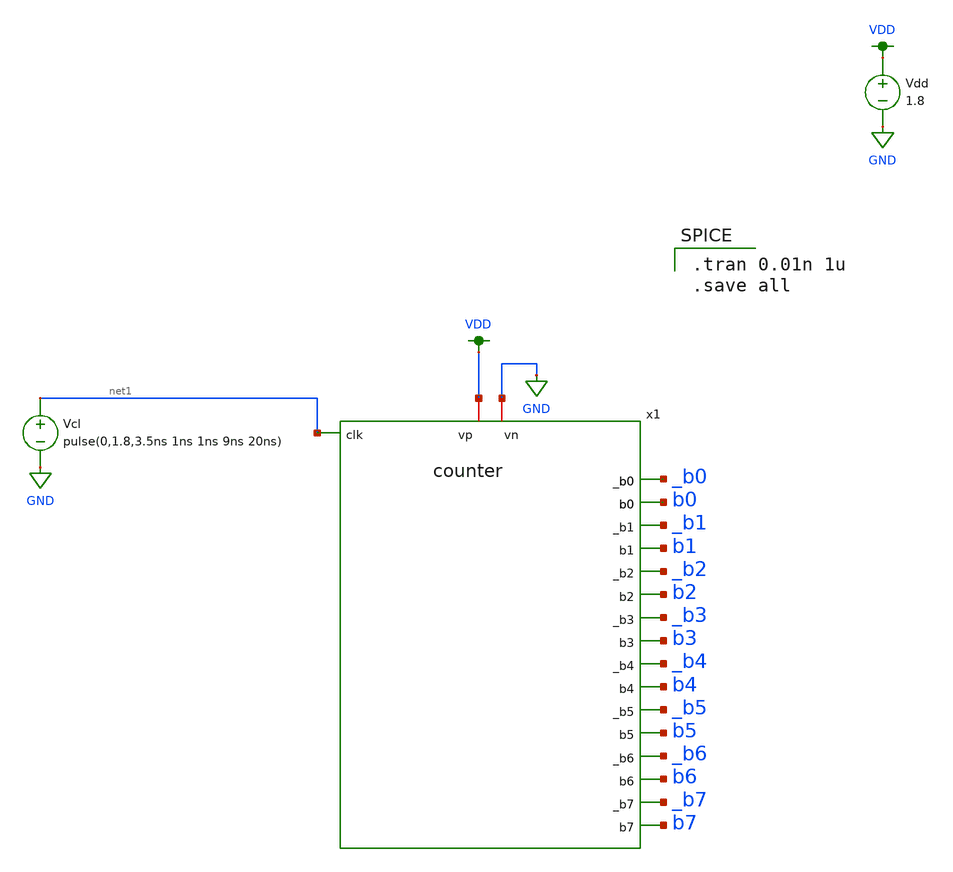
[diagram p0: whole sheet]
** sch_path: xschem/counter_testbench.sch
**.subckt counter_testbench
Vdd VDD GND 1.8
Vcl net1 GND pulse(0,1.8,3.5ns 1ns 1ns 9ns 20ns)
x1 VDD GND net1 _b1 b1 _b2 b2 _b3 b3 _b0 b0 _b5 b5 _b6 b6 _b7 b7 _b4 b4 counter
**** begin user architecture code

.option wnflag=1
.param MC_SWITCH=1.0
.lib ~/skywater/skywater-pdk/libraries/sky130_fd_pr_ngspice/latest/models/sky130.lib.spice tt


.tran 0.01n 1u
.save all

**** end user architecture code
**.ends

* expanding   symbol:  /home/madvlsi/dev/git/magic-dds/xschem/logic_gates/counter.sym # of pins=19
** sym_path: xschem/logic_gates/counter.sym
** sch_path: xschem/logic_gates/counter.sch
.subckt counter vp vn clk _b1 b1 _b2 b2 _b3 b3 _b0 b0 _b5 b5 _b6 b6 _b7 b7 _b4 b4
*.iopin vp
*.iopin vn
*.ipin clk
*.opin b0
*.opin _b0
*.opin b1
*.opin _b1
*.opin b2
*.opin _b2
*.opin b3
*.opin _b3
*.opin b4
*.opin _b4
*.opin b5
*.opin _b5
*.opin b6
*.opin _b6
*.opin b7
*.opin _b7
X2 _b1 b1 _b1 b1 _b0 vp vn dflipflop
X3 _b2 b2 _b2 b2 _b1 vp vn dflipflop
X4 _b3 b3 _b3 b3 _b2 vp vn dflipflop
X5 _b4 b4 _b4 b4 _b3 vp vn dflipflop
X6 _b5 b5 _b5 b5 _b4 vp vn dflipflop
X7 _b6 b6 _b6 b6 _b5 vp vn dflipflop
X8 _b7 b7 _b7 b7 _b6 vp vn dflipflop
x9 vp clk _b0 vn inverter
x10 vp _b0 b0 vn inverter
.ends


* expanding   symbol:  /home/madvlsi/dev/git/magic-dds/xschem/logic_gates/dflipflop.sym # of pins=7
** sym_path: xschem/logic_gates/dflipflop.sym
** sch_path: xschem/logic_gates/dflipflop.sch
.subckt dflipflop q_bar q d d_bar clk vp vn
*.opin q
*.opin q_bar
*.iopin vp
*.iopin vn
*.ipin d_bar
*.ipin d
*.ipin clk
XM8 vp net2 net3 vp sky130_fd_pr__pfet_01v8 L=0.15 W=1 nf=1 ad='int((nf+1)/2) * W/nf * 0.29' as='int((nf+2)/2) * W/nf * 0.29'
+ pd='2*int((nf+1)/2) * (W/nf + 0.29)' ps='2*int((nf+2)/2) * (W/nf + 0.29)' nrd='0.29 / W' nrs='0.29 / W'
+ sa=0 sb=0 sd=0 mult=1 m=1
XM9 vp net3 net2 vp sky130_fd_pr__pfet_01v8 L=0.15 W=1 nf=1 ad='int((nf+1)/2) * W/nf * 0.29' as='int((nf+2)/2) * W/nf * 0.29'
+ pd='2*int((nf+1)/2) * (W/nf + 0.29)' ps='2*int((nf+2)/2) * (W/nf + 0.29)' nrd='0.29 / W' nrs='0.29 / W'
+ sa=0 sb=0 sd=0 mult=1 m=1
XM5 net1 clk vn vn sky130_fd_pr__nfet_01v8 L=0.15 W=1 nf=1 ad='int((nf+1)/2) * W/nf * 0.29' as='int((nf+2)/2) * W/nf * 0.29'
+ pd='2*int((nf+1)/2) * (W/nf + 0.29)' ps='2*int((nf+2)/2) * (W/nf + 0.29)' nrd='0.29 / W' nrs='0.29 / W'
+ sa=0 sb=0 sd=0 mult=1 m=1
XM6 net3 net2 net1 vn sky130_fd_pr__nfet_01v8 L=0.15 W=1 nf=1 ad='int((nf+1)/2) * W/nf * 0.29' as='int((nf+2)/2) * W/nf * 0.29'
+ pd='2*int((nf+1)/2) * (W/nf + 0.29)' ps='2*int((nf+2)/2) * (W/nf + 0.29)' nrd='0.29 / W' nrs='0.29 / W'
+ sa=0 sb=0 sd=0 mult=1 m=1
XM7 net2 net3 net1 vn sky130_fd_pr__nfet_01v8 L=0.15 W=1 nf=1 ad='int((nf+1)/2) * W/nf * 0.29' as='int((nf+2)/2) * W/nf * 0.29'
+ pd='2*int((nf+1)/2) * (W/nf + 0.29)' ps='2*int((nf+2)/2) * (W/nf + 0.29)' nrd='0.29 / W' nrs='0.29 / W'
+ sa=0 sb=0 sd=0 mult=1 m=1
XM13 vn q q_bar vn sky130_fd_pr__nfet_01v8 L=0.15 W=1 nf=1 ad='int((nf+1)/2) * W/nf * 0.29' as='int((nf+2)/2) * W/nf * 0.29'
+ pd='2*int((nf+1)/2) * (W/nf + 0.29)' ps='2*int((nf+2)/2) * (W/nf + 0.29)' nrd='0.29 / W' nrs='0.29 / W'
+ sa=0 sb=0 sd=0 mult=1 m=1
XM3 q clk net2 vn sky130_fd_pr__nfet_01v8 L=0.30 W=1 nf=1 ad='int((nf+1)/2) * W/nf * 0.29' as='int((nf+2)/2) * W/nf * 0.29'
+ pd='2*int((nf+1)/2) * (W/nf + 0.29)' ps='2*int((nf+2)/2) * (W/nf + 0.29)' nrd='0.29 / W' nrs='0.29 / W'
+ sa=0 sb=0 sd=0 mult=1 m=1
XM4 q_bar clk net3 vn sky130_fd_pr__nfet_01v8 L=0.30 W=1 nf=1 ad='int((nf+1)/2) * W/nf * 0.29' as='int((nf+2)/2) * W/nf * 0.29'
+ pd='2*int((nf+1)/2) * (W/nf + 0.29)' ps='2*int((nf+2)/2) * (W/nf + 0.29)' nrd='0.29 / W' nrs='0.29 / W'
+ sa=0 sb=0 sd=0 mult=1 m=1
XM14 vn q_bar q vn sky130_fd_pr__nfet_01v8 L=0.15 W=1 nf=1 ad='int((nf+1)/2) * W/nf * 0.29' as='int((nf+2)/2) * W/nf * 0.29'
+ pd='2*int((nf+1)/2) * (W/nf + 0.29)' ps='2*int((nf+2)/2) * (W/nf + 0.29)' nrd='0.29 / W' nrs='0.29 / W'
+ sa=0 sb=0 sd=0 mult=1 m=1
XM10 net4 clk vp vp sky130_fd_pr__pfet_01v8 L=0.15 W=1 nf=1 ad='int((nf+1)/2) * W/nf * 0.29' as='int((nf+2)/2) * W/nf * 0.29'
+ pd='2*int((nf+1)/2) * (W/nf + 0.29)' ps='2*int((nf+2)/2) * (W/nf + 0.29)' nrd='0.29 / W' nrs='0.29 / W'
+ sa=0 sb=0 sd=0 mult=1 m=1
XM11 q_bar q net4 vp sky130_fd_pr__pfet_01v8 L=0.15 W=1 nf=1 ad='int((nf+1)/2) * W/nf * 0.29' as='int((nf+2)/2) * W/nf * 0.29'
+ pd='2*int((nf+1)/2) * (W/nf + 0.29)' ps='2*int((nf+2)/2) * (W/nf + 0.29)' nrd='0.29 / W' nrs='0.29 / W'
+ sa=0 sb=0 sd=0 mult=1 m=1
XM12 q q_bar net4 vp sky130_fd_pr__pfet_01v8 L=0.15 W=1 nf=1 ad='int((nf+1)/2) * W/nf * 0.29' as='int((nf+2)/2) * W/nf * 0.29'
+ pd='2*int((nf+1)/2) * (W/nf + 0.29)' ps='2*int((nf+2)/2) * (W/nf + 0.29)' nrd='0.29 / W' nrs='0.29 / W'
+ sa=0 sb=0 sd=0 mult=1 m=1
XM15 net1 clk vn vn sky130_fd_pr__nfet_01v8 L=0.15 W=1 nf=1 ad='int((nf+1)/2) * W/nf * 0.29' as='int((nf+2)/2) * W/nf * 0.29'
+ pd='2*int((nf+1)/2) * (W/nf + 0.29)' ps='2*int((nf+2)/2) * (W/nf + 0.29)' nrd='0.29 / W' nrs='0.29 / W'
+ sa=0 sb=0 sd=0 mult=1 m=1
XM16 net4 clk vp vp sky130_fd_pr__pfet_01v8 L=0.15 W=1 nf=1 ad='int((nf+1)/2) * W/nf * 0.29' as='int((nf+2)/2) * W/nf * 0.29'
+ pd='2*int((nf+1)/2) * (W/nf + 0.29)' ps='2*int((nf+2)/2) * (W/nf + 0.29)' nrd='0.29 / W' nrs='0.29 / W'
+ sa=0 sb=0 sd=0 mult=1 m=1
XM1 net2 clk d vp sky130_fd_pr__pfet_01v8 L=0.30 W=1 nf=1 ad='int((nf+1)/2) * W/nf * 0.29' as='int((nf+2)/2) * W/nf * 0.29'
+ pd='2*int((nf+1)/2) * (W/nf + 0.29)' ps='2*int((nf+2)/2) * (W/nf + 0.29)' nrd='0.29 / W' nrs='0.29 / W'
+ sa=0 sb=0 sd=0 mult=1 m=1
XM2 net3 clk d_bar vp sky130_fd_pr__pfet_01v8 L=0.30 W=1 nf=1 ad='int((nf+1)/2) * W/nf * 0.29' as='int((nf+2)/2) * W/nf * 0.29'
+ pd='2*int((nf+1)/2) * (W/nf + 0.29)' ps='2*int((nf+2)/2) * (W/nf + 0.29)' nrd='0.29 / W' nrs='0.29 / W'
+ sa=0 sb=0 sd=0 mult=1 m=1
.ends


* expanding   symbol:  /home/madvlsi/dev/git/magic-dds/xschem/other_project_files/inverter.sym # of
*+ pins=4
** sym_path: xschem/other_project_files/inverter.sym
** sch_path: xschem/other_project_files/inverter.sch
.subckt inverter VP A Y VN
*.iopin VP
*.iopin VN
*.ipin A
*.opin Y
XM1 Y A VN VN sky130_fd_pr__nfet_01v8 L=0.15 W=1 nf=1 ad='int((nf+1)/2) * W/nf * 0.29' as='int((nf+2)/2) * W/nf * 0.29'
+ pd='2*int((nf+1)/2) * (W/nf + 0.29)' ps='2*int((nf+2)/2) * (W/nf + 0.29)' nrd='0.29 / W' nrs='0.29 / W'
+ sa=0 sb=0 sd=0 mult=1 m=1
XM2 Y A VP VP sky130_fd_pr__pfet_01v8 L=0.15 W=4 nf=1 ad='int((nf+1)/2) * W/nf * 0.29' as='int((nf+2)/2) * W/nf * 0.29'
+ pd='2*int((nf+1)/2) * (W/nf + 0.29)' ps='2*int((nf+2)/2) * (W/nf + 0.29)' nrd='0.29 / W' nrs='0.29 / W'
+ sa=0 sb=0 sd=0 mult=1 m=1
.ends

.GLOBAL VDD
.GLOBAL GND
.end
